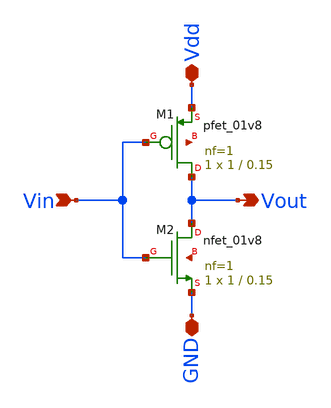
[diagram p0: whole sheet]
** sch_path: xschem/make_symbol_Inverter.sch
**.subckt make_symbol_Inverter Vin Vout Vdd GND
*.ipin Vin
*.opin Vout
*.iopin Vdd
*.iopin GND
XM1 Vout Vin Vdd net1 sky130_fd_pr__pfet_01v8 L=0.15 W=1 nf=1 ad='int((nf+1)/2) * W/nf * 0.29' as='int((nf+2)/2) * W/nf * 0.29'
+ pd='2*int((nf+1)/2) * (W/nf + 0.29)' ps='2*int((nf+2)/2) * (W/nf + 0.29)' nrd='0.29 / W' nrs='0.29 / W'
+ sa=0 sb=0 sd=0 mult=1 m=1
XM2 Vout Vin GND net2 sky130_fd_pr__nfet_01v8 L=0.15 W=1 nf=1 ad='int((nf+1)/2) * W/nf * 0.29' as='int((nf+2)/2) * W/nf * 0.29'
+ pd='2*int((nf+1)/2) * (W/nf + 0.29)' ps='2*int((nf+2)/2) * (W/nf + 0.29)' nrd='0.29 / W' nrs='0.29 / W'
+ sa=0 sb=0 sd=0 mult=1 m=1
**.ends
.end
